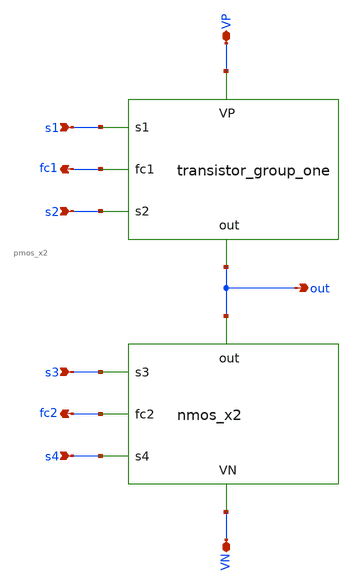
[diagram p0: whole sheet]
** sch_path: xschem/release/power_stage.sch
**.subckt power_stage s1 s2 s3 s4 VP VN out fc1 fc2
*.ipin s1
*.ipin s2
*.ipin s3
*.ipin s4
*.iopin VP
*.iopin VN
*.opin out
*.opin fc1
*.opin fc2
X1 s2 fc1 s1 VP out pmos_x2
X2 s4 fc2 s3 out VN nmos_x2
**.ends
.end
